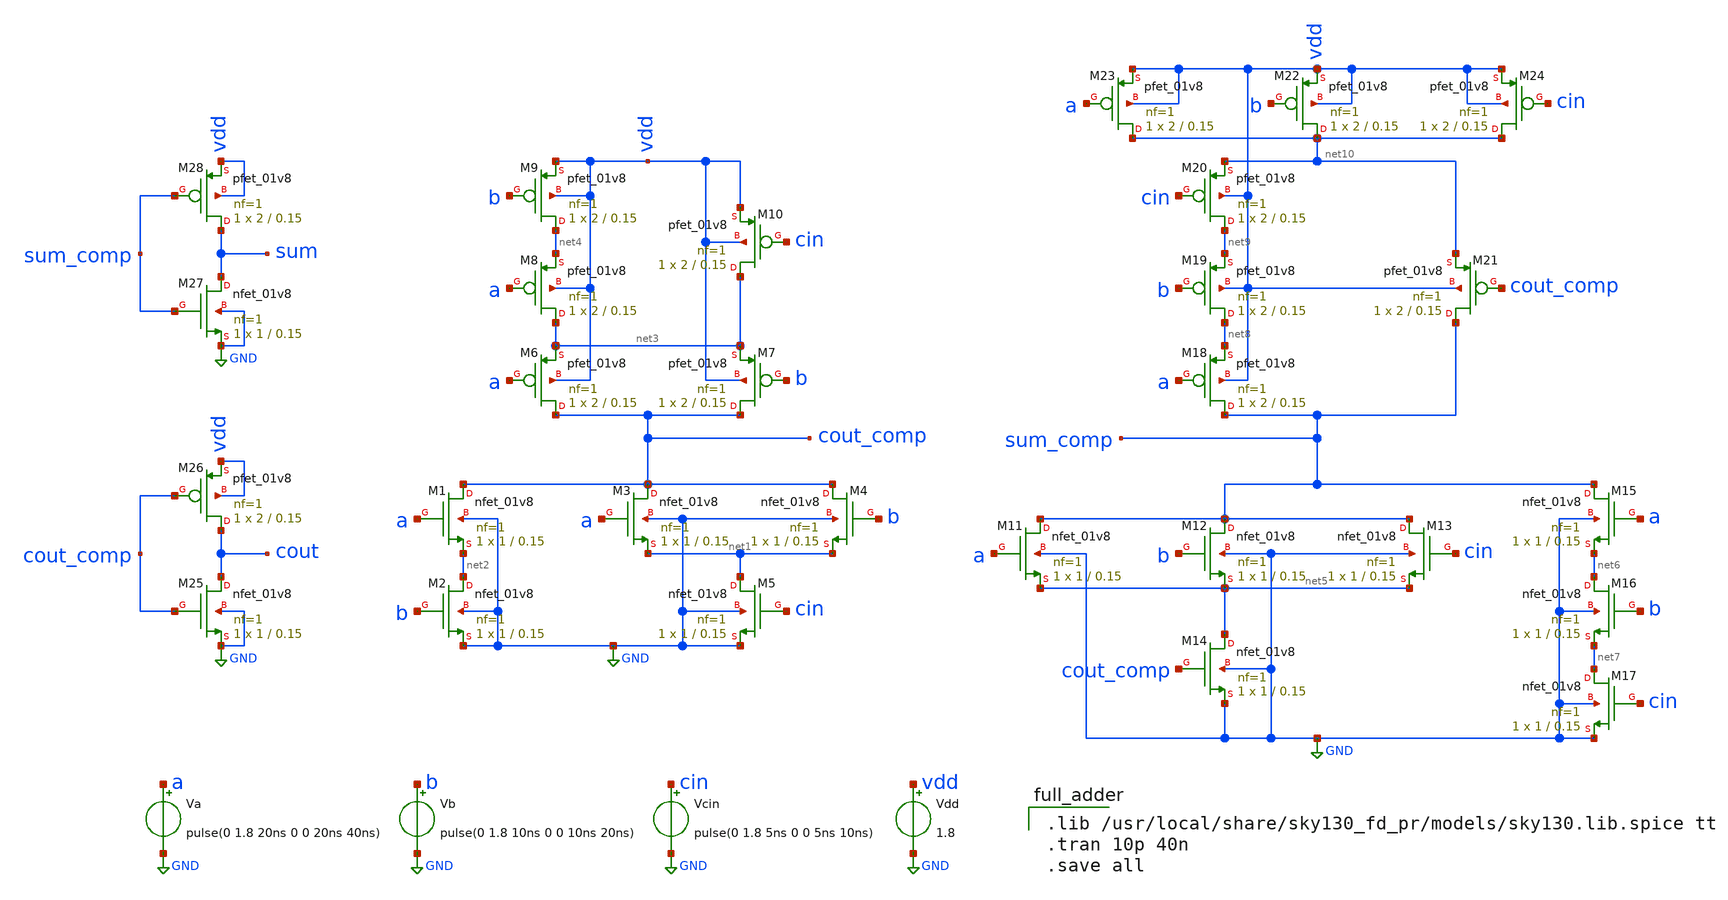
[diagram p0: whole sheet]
** sch_path: files/full_adder.sch
**.subckt full_adder
XM1 cout_comp a net2 GND sky130_fd_pr__nfet_01v8 L=0.15 W=1 nf=1 ad='int((1 + 1)/2) * 1 / 1 * 0.29' as='int((1 + 2)/2) * 1 / 1 * 0.29'
+ pd='2*int((1 + 1)/2) * (1 / 1 + 0.29)' ps='2*int((1 + 2)/2) * (1 / 1 + 0.29)' nrd='0.29 / 1 ' nrs='0.29 / 1 '
+ sa=0 sb=0 sd=0 mult=1 m=1
XM2 net2 b GND GND sky130_fd_pr__nfet_01v8 L=0.15 W=1 nf=1 ad='int((1 + 1)/2) * 1 / 1 * 0.29' as='int((1 + 2)/2) * 1 / 1 * 0.29'
+ pd='2*int((1 + 1)/2) * (1 / 1 + 0.29)' ps='2*int((1 + 2)/2) * (1 / 1 + 0.29)' nrd='0.29 / 1 ' nrs='0.29 / 1 '
+ sa=0 sb=0 sd=0 mult=1 m=1
XM3 cout_comp a net1 GND sky130_fd_pr__nfet_01v8 L=0.15 W=1 nf=1 ad='int((1 + 1)/2) * 1 / 1 * 0.29' as='int((1 + 2)/2) * 1 / 1 * 0.29'
+ pd='2*int((1 + 1)/2) * (1 / 1 + 0.29)' ps='2*int((1 + 2)/2) * (1 / 1 + 0.29)' nrd='0.29 / 1 ' nrs='0.29 / 1 '
+ sa=0 sb=0 sd=0 mult=1 m=1
XM4 cout_comp b net1 GND sky130_fd_pr__nfet_01v8 L=0.15 W=1 nf=1 ad='int((1 + 1)/2) * 1 / 1 * 0.29' as='int((1 + 2)/2) * 1 / 1 * 0.29'
+ pd='2*int((1 + 1)/2) * (1 / 1 + 0.29)' ps='2*int((1 + 2)/2) * (1 / 1 + 0.29)' nrd='0.29 / 1 ' nrs='0.29 / 1 '
+ sa=0 sb=0 sd=0 mult=1 m=1
XM5 net1 cin GND GND sky130_fd_pr__nfet_01v8 L=0.15 W=1 nf=1 ad='int((1 + 1)/2) * 1 / 1 * 0.29' as='int((1 + 2)/2) * 1 / 1 * 0.29'
+ pd='2*int((1 + 1)/2) * (1 / 1 + 0.29)' ps='2*int((1 + 2)/2) * (1 / 1 + 0.29)' nrd='0.29 / 1 ' nrs='0.29 / 1 '
+ sa=0 sb=0 sd=0 mult=1 m=1
XM6 cout_comp a net3 vdd sky130_fd_pr__pfet_01v8 L=0.15 W=2 nf=1 ad='int((1 + 1)/2) * 2 / 1 * 0.29' as='int((1 + 2)/2) * 2 / 1 * 0.29'
+ pd='2*int((1 + 1)/2) * (2 / 1 + 0.29)' ps='2*int((1 + 2)/2) * (2 / 1 + 0.29)' nrd='0.29 / 2 ' nrs='0.29 / 2 '
+ sa=0 sb=0 sd=0 mult=1 m=1
XM7 cout_comp b net3 vdd sky130_fd_pr__pfet_01v8 L=0.15 W=2 nf=1 ad='int((1 + 1)/2) * 2 / 1 * 0.29' as='int((1 + 2)/2) * 2 / 1 * 0.29'
+ pd='2*int((1 + 1)/2) * (2 / 1 + 0.29)' ps='2*int((1 + 2)/2) * (2 / 1 + 0.29)' nrd='0.29 / 2 ' nrs='0.29 / 2 '
+ sa=0 sb=0 sd=0 mult=1 m=1
XM8 net3 a net4 vdd sky130_fd_pr__pfet_01v8 L=0.15 W=2 nf=1 ad='int((1 + 1)/2) * 2 / 1 * 0.29' as='int((1 + 2)/2) * 2 / 1 * 0.29'
+ pd='2*int((1 + 1)/2) * (2 / 1 + 0.29)' ps='2*int((1 + 2)/2) * (2 / 1 + 0.29)' nrd='0.29 / 2 ' nrs='0.29 / 2 '
+ sa=0 sb=0 sd=0 mult=1 m=1
XM9 net4 b vdd vdd sky130_fd_pr__pfet_01v8 L=0.15 W=2 nf=1 ad='int((1 + 1)/2) * 2 / 1 * 0.29' as='int((1 + 2)/2) * 2 / 1 * 0.29'
+ pd='2*int((1 + 1)/2) * (2 / 1 + 0.29)' ps='2*int((1 + 2)/2) * (2 / 1 + 0.29)' nrd='0.29 / 2 ' nrs='0.29 / 2 '
+ sa=0 sb=0 sd=0 mult=1 m=1
XM10 net3 cin vdd vdd sky130_fd_pr__pfet_01v8 L=0.15 W=2 nf=1 ad='int((1 + 1)/2) * 2 / 1 * 0.29' as='int((1 + 2)/2) * 2 / 1 * 0.29'
+ pd='2*int((1 + 1)/2) * (2 / 1 + 0.29)' ps='2*int((1 + 2)/2) * (2 / 1 + 0.29)' nrd='0.29 / 2 ' nrs='0.29 / 2 '
+ sa=0 sb=0 sd=0 mult=1 m=1
Va a GND pulse(0 1.8 20ns 0 0 20ns 40ns)
Vb b GND pulse(0 1.8 10ns 0 0 10ns 20ns)
Vcin cin GND pulse(0 1.8 5ns 0 0 5ns 10ns)
Vdd vdd GND 1.8
XM11 sum_comp a net5 GND sky130_fd_pr__nfet_01v8 L=0.15 W=1 nf=1 ad='int((1 + 1)/2) * 1 / 1 * 0.29' as='int((1 + 2)/2) * 1 / 1 * 0.29'
+ pd='2*int((1 + 1)/2) * (1 / 1 + 0.29)' ps='2*int((1 + 2)/2) * (1 / 1 + 0.29)' nrd='0.29 / 1 ' nrs='0.29 / 1 '
+ sa=0 sb=0 sd=0 mult=1 m=1
XM12 sum_comp b net5 GND sky130_fd_pr__nfet_01v8 L=0.15 W=1 nf=1 ad='int((1 + 1)/2) * 1 / 1 * 0.29' as='int((1 + 2)/2) * 1 / 1 * 0.29'
+ pd='2*int((1 + 1)/2) * (1 / 1 + 0.29)' ps='2*int((1 + 2)/2) * (1 / 1 + 0.29)' nrd='0.29 / 1 ' nrs='0.29 / 1 '
+ sa=0 sb=0 sd=0 mult=1 m=1
XM13 sum_comp cin net5 GND sky130_fd_pr__nfet_01v8 L=0.15 W=1 nf=1 ad='int((1 + 1)/2) * 1 / 1 * 0.29'
+ as='int((1 + 2)/2) * 1 / 1 * 0.29' pd='2*int((1 + 1)/2) * (1 / 1 + 0.29)' ps='2*int((1 + 2)/2) * (1 / 1 + 0.29)'
+ nrd='0.29 / 1 ' nrs='0.29 / 1 ' sa=0 sb=0 sd=0 mult=1 m=1
XM14 net5 cout_comp GND GND sky130_fd_pr__nfet_01v8 L=0.15 W=1 nf=1 ad='int((1 + 1)/2) * 1 / 1 * 0.29'
+ as='int((1 + 2)/2) * 1 / 1 * 0.29' pd='2*int((1 + 1)/2) * (1 / 1 + 0.29)' ps='2*int((1 + 2)/2) * (1 / 1 + 0.29)'
+ nrd='0.29 / 1 ' nrs='0.29 / 1 ' sa=0 sb=0 sd=0 mult=1 m=1
XM15 sum_comp a net6 GND sky130_fd_pr__nfet_01v8 L=0.15 W=1 nf=1 ad='int((1 + 1)/2) * 1 / 1 * 0.29' as='int((1 + 2)/2) * 1 / 1 * 0.29'
+ pd='2*int((1 + 1)/2) * (1 / 1 + 0.29)' ps='2*int((1 + 2)/2) * (1 / 1 + 0.29)' nrd='0.29 / 1 ' nrs='0.29 / 1 '
+ sa=0 sb=0 sd=0 mult=1 m=1
XM16 net6 b net7 GND sky130_fd_pr__nfet_01v8 L=0.15 W=1 nf=1 ad='int((1 + 1)/2) * 1 / 1 * 0.29' as='int((1 + 2)/2) * 1 / 1 * 0.29'
+ pd='2*int((1 + 1)/2) * (1 / 1 + 0.29)' ps='2*int((1 + 2)/2) * (1 / 1 + 0.29)' nrd='0.29 / 1 ' nrs='0.29 / 1 '
+ sa=0 sb=0 sd=0 mult=1 m=1
XM17 net7 cin GND GND sky130_fd_pr__nfet_01v8 L=0.15 W=1 nf=1 ad='int((1 + 1)/2) * 1 / 1 * 0.29' as='int((1 + 2)/2) * 1 / 1 * 0.29'
+ pd='2*int((1 + 1)/2) * (1 / 1 + 0.29)' ps='2*int((1 + 2)/2) * (1 / 1 + 0.29)' nrd='0.29 / 1 ' nrs='0.29 / 1 '
+ sa=0 sb=0 sd=0 mult=1 m=1
XM18 sum_comp a net8 vdd sky130_fd_pr__pfet_01v8 L=0.15 W=2 nf=1 ad='int((1 + 1)/2) * 2 / 1 * 0.29' as='int((1 + 2)/2) * 2 / 1 * 0.29'
+ pd='2*int((1 + 1)/2) * (2 / 1 + 0.29)' ps='2*int((1 + 2)/2) * (2 / 1 + 0.29)' nrd='0.29 / 2 ' nrs='0.29 / 2 '
+ sa=0 sb=0 sd=0 mult=1 m=1
XM19 net8 b net9 vdd sky130_fd_pr__pfet_01v8 L=0.15 W=2 nf=1 ad='int((1 + 1)/2) * 2 / 1 * 0.29' as='int((1 + 2)/2) * 2 / 1 * 0.29'
+ pd='2*int((1 + 1)/2) * (2 / 1 + 0.29)' ps='2*int((1 + 2)/2) * (2 / 1 + 0.29)' nrd='0.29 / 2 ' nrs='0.29 / 2 '
+ sa=0 sb=0 sd=0 mult=1 m=1
XM20 net9 cin net10 vdd sky130_fd_pr__pfet_01v8 L=0.15 W=2 nf=1 ad='int((1 + 1)/2) * 2 / 1 * 0.29' as='int((1 + 2)/2) * 2 / 1 * 0.29'
+ pd='2*int((1 + 1)/2) * (2 / 1 + 0.29)' ps='2*int((1 + 2)/2) * (2 / 1 + 0.29)' nrd='0.29 / 2 ' nrs='0.29 / 2 '
+ sa=0 sb=0 sd=0 mult=1 m=1
XM22 net10 b vdd vdd sky130_fd_pr__pfet_01v8 L=0.15 W=2 nf=1 ad='int((1 + 1)/2) * 2 / 1 * 0.29' as='int((1 + 2)/2) * 2 / 1 * 0.29'
+ pd='2*int((1 + 1)/2) * (2 / 1 + 0.29)' ps='2*int((1 + 2)/2) * (2 / 1 + 0.29)' nrd='0.29 / 2 ' nrs='0.29 / 2 '
+ sa=0 sb=0 sd=0 mult=1 m=1
XM23 net10 a vdd vdd sky130_fd_pr__pfet_01v8 L=0.15 W=2 nf=1 ad='int((1 + 1)/2) * 2 / 1 * 0.29' as='int((1 + 2)/2) * 2 / 1 * 0.29'
+ pd='2*int((1 + 1)/2) * (2 / 1 + 0.29)' ps='2*int((1 + 2)/2) * (2 / 1 + 0.29)' nrd='0.29 / 2 ' nrs='0.29 / 2 '
+ sa=0 sb=0 sd=0 mult=1 m=1
XM24 net10 cin vdd vdd sky130_fd_pr__pfet_01v8 L=0.15 W=2 nf=1 ad='int((1 + 1)/2) * 2 / 1 * 0.29' as='int((1 + 2)/2) * 2 / 1 * 0.29'
+ pd='2*int((1 + 1)/2) * (2 / 1 + 0.29)' ps='2*int((1 + 2)/2) * (2 / 1 + 0.29)' nrd='0.29 / 2 ' nrs='0.29 / 2 '
+ sa=0 sb=0 sd=0 mult=1 m=1
XM25 cout cout_comp GND GND sky130_fd_pr__nfet_01v8 L=0.15 W=1 nf=1 ad='int((1 + 1)/2) * 1 / 1 * 0.29'
+ as='int((1 + 2)/2) * 1 / 1 * 0.29' pd='2*int((1 + 1)/2) * (1 / 1 + 0.29)' ps='2*int((1 + 2)/2) * (1 / 1 + 0.29)'
+ nrd='0.29 / 1 ' nrs='0.29 / 1 ' sa=0 sb=0 sd=0 mult=1 m=1
XM26 cout cout_comp vdd vdd sky130_fd_pr__pfet_01v8 L=0.15 W=2 nf=1 ad='int((1 + 1)/2) * 2 / 1 * 0.29'
+ as='int((1 + 2)/2) * 2 / 1 * 0.29' pd='2*int((1 + 1)/2) * (2 / 1 + 0.29)' ps='2*int((1 + 2)/2) * (2 / 1 + 0.29)'
+ nrd='0.29 / 2 ' nrs='0.29 / 2 ' sa=0 sb=0 sd=0 mult=1 m=1
XM27 sum sum_comp GND GND sky130_fd_pr__nfet_01v8 L=0.15 W=1 nf=1 ad='int((1 + 1)/2) * 1 / 1 * 0.29'
+ as='int((1 + 2)/2) * 1 / 1 * 0.29' pd='2*int((1 + 1)/2) * (1 / 1 + 0.29)' ps='2*int((1 + 2)/2) * (1 / 1 + 0.29)'
+ nrd='0.29 / 1 ' nrs='0.29 / 1 ' sa=0 sb=0 sd=0 mult=1 m=1
XM28 sum sum_comp vdd vdd sky130_fd_pr__pfet_01v8 L=0.15 W=2 nf=1 ad='int((1 + 1)/2) * 2 / 1 * 0.29'
+ as='int((1 + 2)/2) * 2 / 1 * 0.29' pd='2*int((1 + 1)/2) * (2 / 1 + 0.29)' ps='2*int((1 + 2)/2) * (2 / 1 + 0.29)'
+ nrd='0.29 / 2 ' nrs='0.29 / 2 ' sa=0 sb=0 sd=0 mult=1 m=1
XM21 sum_comp cout_comp net10 vdd sky130_fd_pr__pfet_01v8 L=0.15 W=2 nf=1 ad='int((1 + 1)/2) * 2 / 1 * 0.29'
+ as='int((1 + 2)/2) * 2 / 1 * 0.29' pd='2*int((1 + 1)/2) * (2 / 1 + 0.29)' ps='2*int((1 + 2)/2) * (2 / 1 + 0.29)'
+ nrd='0.29 / 2 ' nrs='0.29 / 2 ' sa=0 sb=0 sd=0 mult=1 m=1
**** begin user architecture code

.lib /usr/local/share/sky130_fd_pr/models/sky130.lib.spice tt
.tran 10p 40n
.save all

**** end user architecture code
**.ends
.GLOBAL GND
.end
